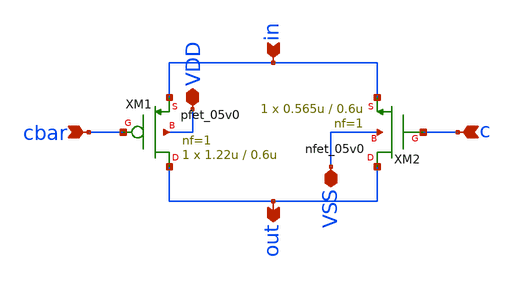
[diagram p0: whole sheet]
** sch_path: TGATE/TGATE.sch
**.subckt TGATE in out cbar c VDD VSS
*.ipin in
*.opin out
*.ipin cbar
*.ipin c
*.iopin VDD
*.iopin VSS
XM1 out cbar in VDD pfet_05v0 L=0.6u W=1.22u nf=1 ad='int((nf+1)/2) * W/nf * 0.18u' as='int((nf+2)/2) * W/nf * 0.18u'
+ pd='2*int((nf+1)/2) * (W/nf + 0.18u)' ps='2*int((nf+2)/2) * (W/nf + 0.18u)' nrd='0.18u / W' nrs='0.18u / W'
+ sa=0 sb=0 sd=0 m=1
XM2 out c in VSS nfet_05v0 L=0.6u W=0.565u nf=1 ad='int((nf+1)/2) * W/nf * 0.18u' as='int((nf+2)/2) * W/nf * 0.18u'
+ pd='2*int((nf+1)/2) * (W/nf + 0.18u)' ps='2*int((nf+2)/2) * (W/nf + 0.18u)' nrd='0.18u / W' nrs='0.18u / W'
+ sa=0 sb=0 sd=0 m=1
**.ends
.end
